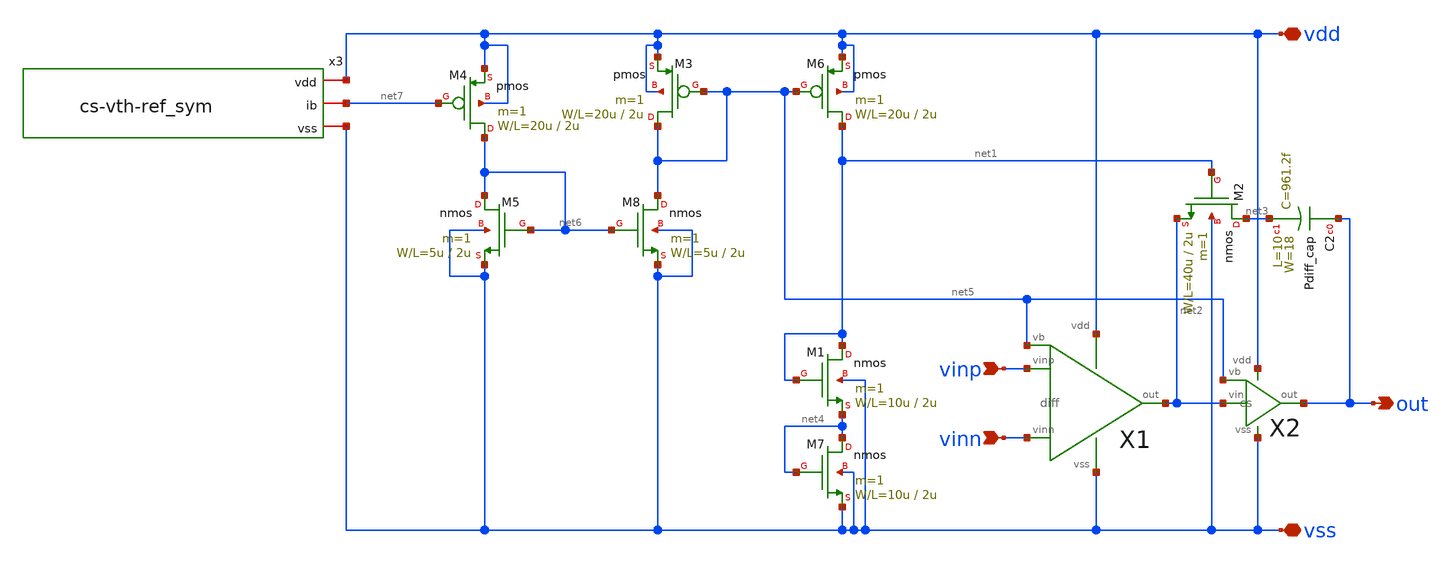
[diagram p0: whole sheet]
** sch_path: OR1/PTC06/opamp/opamp_cs.sch
**.subckt opamp_cs vinp vinn out vdd vss
*.ipin vinp
*.ipin vinn
*.opin out
*.iopin vdd
*.iopin vss
X1 vinp vinn net2 vdd vss net5 diff
X2 net2 net5 out vdd vss cs
M3 net5 net5 vdd vdd pmos L=2u W=20u m=1
M2 net3 net1 net2 vss nmos L=2u W=40u m=1
M6 net1 net5 vdd vdd pmos L=2u W=20u m=1
M1 net1 net1 net4 vss nmos L=2u W=10u m=1
M7 net4 net4 vss vss nmos L=2u W=10u m=1
x3 vdd net7 vss cs-vth-ref_sym
M4 net6 net7 vdd vdd pmos L=2u W=20u m=1
M5 net6 net6 vss vss nmos L=2u W=5u m=1
M8 net5 net6 vss vss nmos L=2u W=5u m=1
C2 out net3 Pdiff_cap W=18 L=10
**.ends

* expanding   symbol:  diff.sym # of pins=6
** sym_path: diff.sym
** sch_path: diff.sch
.subckt diff vinp vinn out vdd vss vb
*.ipin vinn
*.ipin vinp
*.ipin vb
*.opin out
*.iopin vdd
*.iopin vss
M5 net2 vb vdd vdd pmos L=2u W=40u m=1
M1 net1 vinn net2 net2 pmos L=2u W=200u m=1
M2 out vinp net2 net2 pmos L=2u W=200u m=1
M3 net1 net1 vss vss nmos L=2u W=10u m=1
M4 out net1 vss vss nmos L=2u W=10u m=1
.ends


* expanding   symbol:  cs.sym # of pins=5
** sym_path: cs.sym
** sch_path: cs.sch
.subckt cs vin vb out vdd vss
*.ipin vb
*.ipin vin
*.opin out
*.iopin vss
*.iopin vdd
M6 out vb vdd vdd pmos L=2u W=400u m=1
M7 out vin vss vss nmos L=2u W=200u m=1
.ends


* expanding   symbol:  cs-vth-ref_sym.sym # of pins=3
** sym_path: cs-vth-ref_sym.sym
** sch_path: cs-vth-ref_sym.sch
.subckt cs-vth-ref_sym vdd ib vss
*.iopin vdd
*.iopin vss
*.iopin ib
R2 vss net2 HR_poly W=2.0 L=2000
M4 ib ib vdd vdd pmos L=2u W=100u m=1
M3 net1 ib vdd vdd pmos L=2u W=100u m=1
M2 ib net1 net2 vss nmos L=2u W=20u m=1
M1 net1 net2 vss vss nmos L=2u W=20u m=1
.ends

.end
